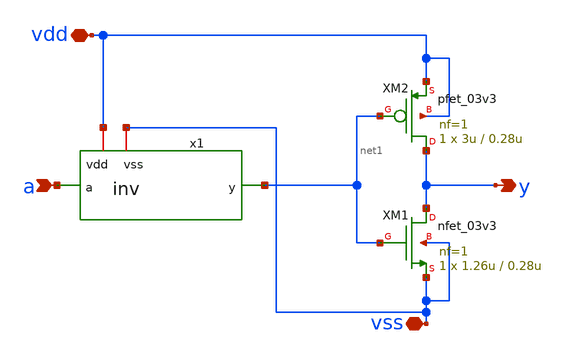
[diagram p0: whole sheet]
** sch_path: member_project/ice458/dynamic_comparator/xschem/out_buf.sch
**.subckt out_buf vdd vss a y
*.iopin vdd
*.iopin vss
*.ipin a
*.opin y
XM1 y net1 vss vss nfet_03v3 L=0.28u W=1.26u nf=1 ad='int((nf+1)/2) * W/nf * 0.18u' as='int((nf+2)/2) * W/nf * 0.18u'
+ pd='2*int((nf+1)/2) * (W/nf + 0.18u)' ps='2*int((nf+2)/2) * (W/nf + 0.18u)' nrd='0.18u / W' nrs='0.18u / W'
+ sa=0 sb=0 sd=0 m=1
XM2 y net1 vdd vdd pfet_03v3 L=0.28u W=3u nf=1 ad='int((nf+1)/2) * W/nf * 0.18u' as='int((nf+2)/2) * W/nf * 0.18u'
+ pd='2*int((nf+1)/2) * (W/nf + 0.18u)' ps='2*int((nf+2)/2) * (W/nf + 0.18u)' nrd='0.18u / W' nrs='0.18u / W'
+ sa=0 sb=0 sd=0 m=1
x1 vdd a net1 vss inv
**.ends

* expanding   symbol:  inv.sym # of pins=4
** sym_path: member_project/ice458/dynamic_comparator/xschem/inv.sym
** sch_path: member_project/ice458/dynamic_comparator/xschem/inv.sch
.subckt inv vdd a y vss
*.iopin vdd
*.iopin vss
*.ipin a
*.opin y
XM1 y a vss vss nfet_03v3 L=0.28u W=0.42u nf=1 ad='int((nf+1)/2) * W/nf * 0.18u' as='int((nf+2)/2) * W/nf * 0.18u'
+ pd='2*int((nf+1)/2) * (W/nf + 0.18u)' ps='2*int((nf+2)/2) * (W/nf + 0.18u)' nrd='0.18u / W' nrs='0.18u / W'
+ sa=0 sb=0 sd=0 m=1
XM2 y a vdd vdd pfet_03v3 L=0.28u W=1u nf=1 ad='int((nf+1)/2) * W/nf * 0.18u' as='int((nf+2)/2) * W/nf * 0.18u'
+ pd='2*int((nf+1)/2) * (W/nf + 0.18u)' ps='2*int((nf+2)/2) * (W/nf + 0.18u)' nrd='0.18u / W' nrs='0.18u / W'
+ sa=0 sb=0 sd=0 m=1
.ends

.end
